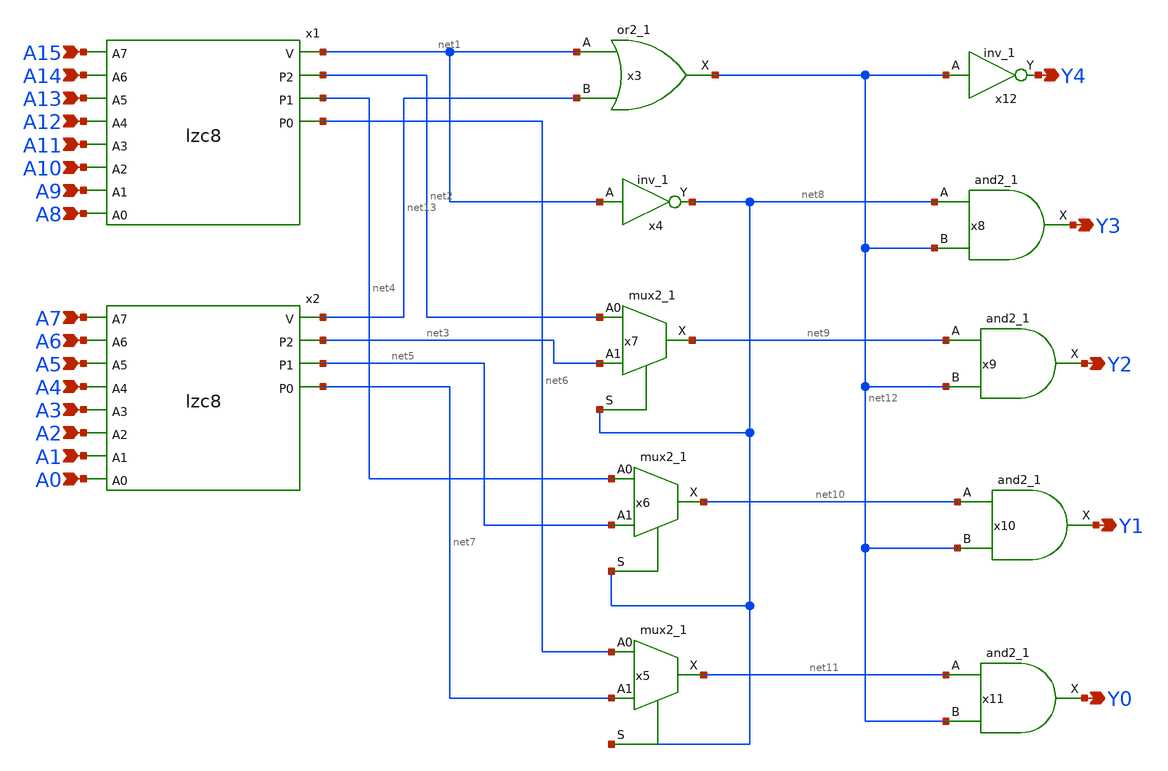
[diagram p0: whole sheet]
** sch_path: frontend/xschem/lzc16.sch
**.subckt lzc16 A15 A14 A13 A12 A11 A10 A9 A8 A7 A6 A5 A4 A3 A2 A1 A0 Y4 Y3 Y2 Y1 Y0
*.ipin A15
*.ipin A14
*.ipin A13
*.ipin A12
*.ipin A11
*.ipin A10
*.ipin A9
*.ipin A8
*.ipin A7
*.ipin A6
*.ipin A5
*.ipin A4
*.ipin A3
*.ipin A2
*.ipin A1
*.ipin A0
*.opin Y4
*.opin Y3
*.opin Y2
*.opin Y1
*.opin Y0
x1 A15 A14 net1 A13 A12 net2 A11 A10 net4 A9 A8 net6 lzc8
x2 A7 A6 net13 A5 A4 net3 A3 A2 net5 A1 A0 net7 lzc8
x3 net1 net13 VGND VNB VPB VPWR net12 sky130_fd_sc_hd__or2_1
x4 net1 VGND VNB VPB VPWR net8 sky130_fd_sc_hd__inv_1
x5 net6 net7 net8 VGND VNB VPB VPWR net11 sky130_fd_sc_hd__mux2_1
x6 net4 net5 net8 VGND VNB VPB VPWR net10 sky130_fd_sc_hd__mux2_1
x7 net2 net3 net8 VGND VNB VPB VPWR net9 sky130_fd_sc_hd__mux2_1
x8 net8 net12 VGND VNB VPB VPWR Y3 sky130_fd_sc_hd__and2_1
x9 net9 net12 VGND VNB VPB VPWR Y2 sky130_fd_sc_hd__and2_1
x10 net10 net12 VGND VNB VPB VPWR Y1 sky130_fd_sc_hd__and2_1
x11 net11 net12 VGND VNB VPB VPWR Y0 sky130_fd_sc_hd__and2_1
x12 net12 VGND VNB VPB VPWR Y4 sky130_fd_sc_hd__inv_1
**.ends

* expanding   symbol:  lzc8.sym # of pins=12
** sym_path: frontend/xschem/lzc8.sym
** sch_path: frontend/xschem/lzc8.sch
.subckt lzc8 A7 A6 V A5 A4 P2 A3 A2 P1 A1 A0 P0
*.ipin A7
*.ipin A6
*.ipin A5
*.ipin A4
*.ipin A3
*.ipin A2
*.ipin A1
*.ipin A0
*.opin V
*.opin P2
*.opin P1
*.opin P0
x1 A7 net1 A6 net2 A5 A4 net5 lzc4
x2 A3 net3 A2 net4 A1 A0 net6 lzc4
x3 net1 net3 VGND VNB VPB VPWR V sky130_fd_sc_hd__or2_1
x4 net1 VGND VNB VPB VPWR P2 sky130_fd_sc_hd__inv_1
x5 net2 net4 P2 VGND VNB VPB VPWR P1 sky130_fd_sc_hd__mux2_1
x6 net5 net6 P2 VGND VNB VPB VPWR P0 sky130_fd_sc_hd__mux2_1
.ends


* expanding   symbol:  lzc4.sym # of pins=7
** sym_path: frontend/xschem/lzc4.sym
** sch_path: frontend/xschem/lzc4.sch
.subckt lzc4 A3 V A2 P1 A1 A0 P0
*.ipin A3
*.ipin A2
*.ipin A1
*.ipin A0
*.opin V
*.opin P1
*.opin P0
x1 A3 net1 A2 net3 lzc2
x2 A1 net2 A0 net4 lzc2
x3 net1 net2 VGND VNB VPB VPWR V sky130_fd_sc_hd__or2_1
x4 net1 VGND VNB VPB VPWR P1 sky130_fd_sc_hd__inv_1
x5 net3 net4 P1 VGND VNB VPB VPWR P0 sky130_fd_sc_hd__mux2_1
.ends


* expanding   symbol:  lzc2.sym # of pins=4
** sym_path: frontend/xschem/lzc2.sym
** sch_path: frontend/xschem/lzc2.sch
.subckt lzc2 HI V LO P
*.ipin HI
*.ipin LO
*.opin V
*.opin P
x1 HI LO VGND VNB VPB VPWR V sky130_fd_sc_hd__or2_1
x2 HI GND GND VDD VDD P sky130_fd_sc_hd__inv_1
.ends

.end
